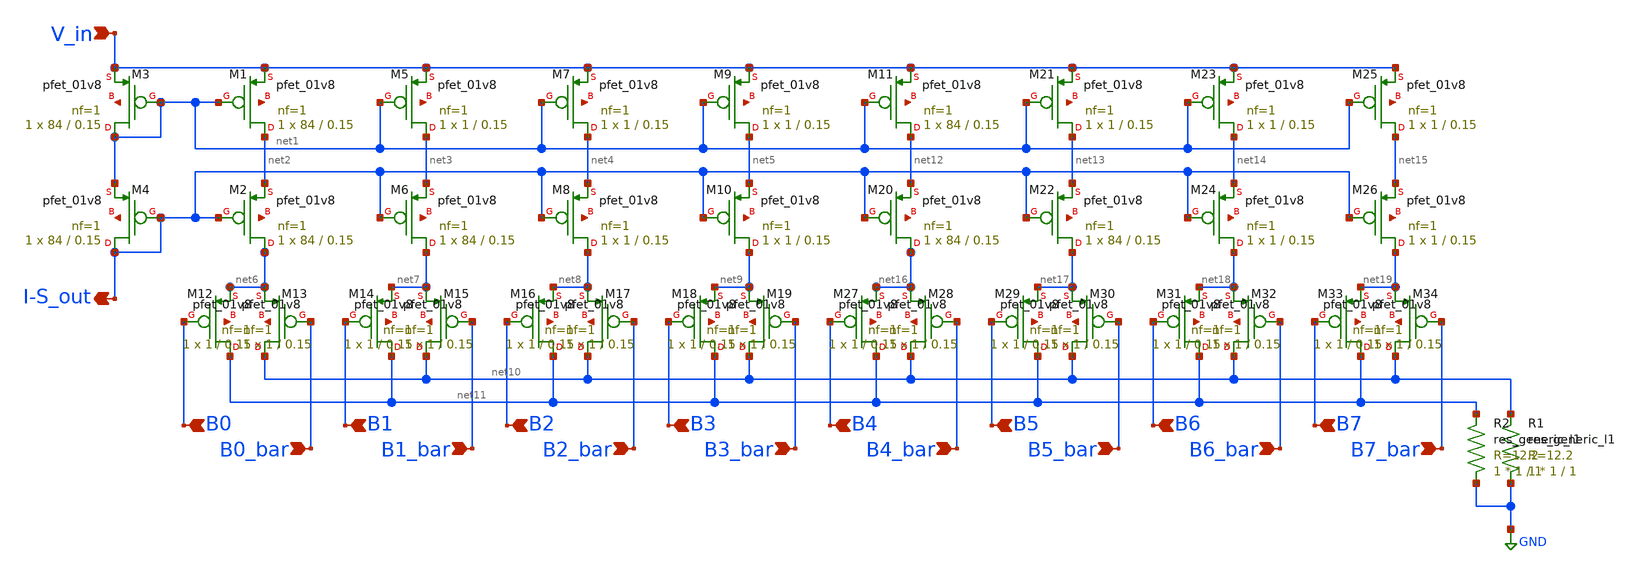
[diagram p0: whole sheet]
** sch_path: analog/schematics/DAC.sch
**.subckt DAC V_in I-S_out B0 V_in B0_bar B1 B2 B3 B1_bar B2_bar B3_bar B4 B4_bar B5 B6 B7 B5_bar
*+ B6_bar B7_bar
*.ipin V_in
*.opin I-S_out
*.ipin B0
*.ipin V_in
*.ipin B0_bar
*.ipin B1
*.ipin B2
*.ipin B3
*.ipin B1_bar
*.ipin B2_bar
*.ipin B3_bar
*.ipin B4
*.ipin B4_bar
*.ipin B5
*.ipin B6
*.ipin B7
*.ipin B5_bar
*.ipin B6_bar
*.ipin B7_bar
XM1 net2 net1 V_in net20 sky130_fd_pr__pfet_01v8 L=0.15 W=84 nf=1 ad='int((nf+1)/2) * W/nf * 0.29' as='int((nf+2)/2) * W/nf * 0.29'
+ pd='2*int((nf+1)/2) * (W/nf + 0.29)' ps='2*int((nf+2)/2) * (W/nf + 0.29)' nrd='0.29 / W' nrs='0.29 / W'
+ sa=0 sb=0 sd=0 mult=1 m=1
XM2 net6 I-S_out net2 net21 sky130_fd_pr__pfet_01v8 L=0.15 W=84 nf=1 ad='int((nf+1)/2) * W/nf * 0.29'
+ as='int((nf+2)/2) * W/nf * 0.29' pd='2*int((nf+1)/2) * (W/nf + 0.29)' ps='2*int((nf+2)/2) * (W/nf + 0.29)'
+ nrd='0.29 / W' nrs='0.29 / W' sa=0 sb=0 sd=0 mult=1 m=1
XM3 net1 net1 V_in net22 sky130_fd_pr__pfet_01v8 L=0.15 W=84 nf=1 ad='int((nf+1)/2) * W/nf * 0.29' as='int((nf+2)/2) * W/nf * 0.29'
+ pd='2*int((nf+1)/2) * (W/nf + 0.29)' ps='2*int((nf+2)/2) * (W/nf + 0.29)' nrd='0.29 / W' nrs='0.29 / W'
+ sa=0 sb=0 sd=0 mult=1 m=1
XM4 I-S_out I-S_out net1 net23 sky130_fd_pr__pfet_01v8 L=0.15 W=84 nf=1 ad='int((nf+1)/2) * W/nf * 0.29'
+ as='int((nf+2)/2) * W/nf * 0.29' pd='2*int((nf+1)/2) * (W/nf + 0.29)' ps='2*int((nf+2)/2) * (W/nf + 0.29)'
+ nrd='0.29 / W' nrs='0.29 / W' sa=0 sb=0 sd=0 mult=1 m=1
XM5 net3 net1 V_in net24 sky130_fd_pr__pfet_01v8 L=0.15 W=1 nf=1 ad='int((nf+1)/2) * W/nf * 0.29' as='int((nf+2)/2) * W/nf * 0.29'
+ pd='2*int((nf+1)/2) * (W/nf + 0.29)' ps='2*int((nf+2)/2) * (W/nf + 0.29)' nrd='0.29 / W' nrs='0.29 / W'
+ sa=0 sb=0 sd=0 mult=1 m=1
XM6 net7 I-S_out net3 net25 sky130_fd_pr__pfet_01v8 L=0.15 W=84 nf=1 ad='int((nf+1)/2) * W/nf * 0.29'
+ as='int((nf+2)/2) * W/nf * 0.29' pd='2*int((nf+1)/2) * (W/nf + 0.29)' ps='2*int((nf+2)/2) * (W/nf + 0.29)'
+ nrd='0.29 / W' nrs='0.29 / W' sa=0 sb=0 sd=0 mult=1 m=1
XM7 net4 net1 V_in net26 sky130_fd_pr__pfet_01v8 L=0.15 W=1 nf=1 ad='int((nf+1)/2) * W/nf * 0.29' as='int((nf+2)/2) * W/nf * 0.29'
+ pd='2*int((nf+1)/2) * (W/nf + 0.29)' ps='2*int((nf+2)/2) * (W/nf + 0.29)' nrd='0.29 / W' nrs='0.29 / W'
+ sa=0 sb=0 sd=0 mult=1 m=1
XM8 net8 I-S_out net4 net27 sky130_fd_pr__pfet_01v8 L=0.15 W=1 nf=1 ad='int((nf+1)/2) * W/nf * 0.29'
+ as='int((nf+2)/2) * W/nf * 0.29' pd='2*int((nf+1)/2) * (W/nf + 0.29)' ps='2*int((nf+2)/2) * (W/nf + 0.29)'
+ nrd='0.29 / W' nrs='0.29 / W' sa=0 sb=0 sd=0 mult=1 m=1
XM9 net5 net1 V_in net28 sky130_fd_pr__pfet_01v8 L=0.15 W=1 nf=1 ad='int((nf+1)/2) * W/nf * 0.29' as='int((nf+2)/2) * W/nf * 0.29'
+ pd='2*int((nf+1)/2) * (W/nf + 0.29)' ps='2*int((nf+2)/2) * (W/nf + 0.29)' nrd='0.29 / W' nrs='0.29 / W'
+ sa=0 sb=0 sd=0 mult=1 m=1
XM10 net9 I-S_out net5 net29 sky130_fd_pr__pfet_01v8 L=0.15 W=1 nf=1 ad='int((nf+1)/2) * W/nf * 0.29'
+ as='int((nf+2)/2) * W/nf * 0.29' pd='2*int((nf+1)/2) * (W/nf + 0.29)' ps='2*int((nf+2)/2) * (W/nf + 0.29)'
+ nrd='0.29 / W' nrs='0.29 / W' sa=0 sb=0 sd=0 mult=1 m=1
XM12 net11 B0 net6 net30 sky130_fd_pr__pfet_01v8 L=0.15 W=1 nf=1 ad='int((nf+1)/2) * W/nf * 0.29' as='int((nf+2)/2) * W/nf * 0.29'
+ pd='2*int((nf+1)/2) * (W/nf + 0.29)' ps='2*int((nf+2)/2) * (W/nf + 0.29)' nrd='0.29 / W' nrs='0.29 / W'
+ sa=0 sb=0 sd=0 mult=1 m=1
XM13 net10 B0_bar net6 net31 sky130_fd_pr__pfet_01v8 L=0.15 W=1 nf=1 ad='int((nf+1)/2) * W/nf * 0.29'
+ as='int((nf+2)/2) * W/nf * 0.29' pd='2*int((nf+1)/2) * (W/nf + 0.29)' ps='2*int((nf+2)/2) * (W/nf + 0.29)'
+ nrd='0.29 / W' nrs='0.29 / W' sa=0 sb=0 sd=0 mult=1 m=1
XM14 net11 B1 net7 net32 sky130_fd_pr__pfet_01v8 L=0.15 W=1 nf=1 ad='int((nf+1)/2) * W/nf * 0.29' as='int((nf+2)/2) * W/nf * 0.29'
+ pd='2*int((nf+1)/2) * (W/nf + 0.29)' ps='2*int((nf+2)/2) * (W/nf + 0.29)' nrd='0.29 / W' nrs='0.29 / W'
+ sa=0 sb=0 sd=0 mult=1 m=1
XM15 net10 B1_bar net7 net33 sky130_fd_pr__pfet_01v8 L=0.15 W=1 nf=1 ad='int((nf+1)/2) * W/nf * 0.29'
+ as='int((nf+2)/2) * W/nf * 0.29' pd='2*int((nf+1)/2) * (W/nf + 0.29)' ps='2*int((nf+2)/2) * (W/nf + 0.29)'
+ nrd='0.29 / W' nrs='0.29 / W' sa=0 sb=0 sd=0 mult=1 m=1
XM16 net11 B2 net8 net34 sky130_fd_pr__pfet_01v8 L=0.15 W=1 nf=1 ad='int((nf+1)/2) * W/nf * 0.29' as='int((nf+2)/2) * W/nf * 0.29'
+ pd='2*int((nf+1)/2) * (W/nf + 0.29)' ps='2*int((nf+2)/2) * (W/nf + 0.29)' nrd='0.29 / W' nrs='0.29 / W'
+ sa=0 sb=0 sd=0 mult=1 m=1
XM17 net10 B2_bar net8 net35 sky130_fd_pr__pfet_01v8 L=0.15 W=1 nf=1 ad='int((nf+1)/2) * W/nf * 0.29'
+ as='int((nf+2)/2) * W/nf * 0.29' pd='2*int((nf+1)/2) * (W/nf + 0.29)' ps='2*int((nf+2)/2) * (W/nf + 0.29)'
+ nrd='0.29 / W' nrs='0.29 / W' sa=0 sb=0 sd=0 mult=1 m=1
XM18 net11 B3 net9 net36 sky130_fd_pr__pfet_01v8 L=0.15 W=1 nf=1 ad='int((nf+1)/2) * W/nf * 0.29' as='int((nf+2)/2) * W/nf * 0.29'
+ pd='2*int((nf+1)/2) * (W/nf + 0.29)' ps='2*int((nf+2)/2) * (W/nf + 0.29)' nrd='0.29 / W' nrs='0.29 / W'
+ sa=0 sb=0 sd=0 mult=1 m=1
XM19 net10 B3_bar net9 net37 sky130_fd_pr__pfet_01v8 L=0.15 W=1 nf=1 ad='int((nf+1)/2) * W/nf * 0.29'
+ as='int((nf+2)/2) * W/nf * 0.29' pd='2*int((nf+1)/2) * (W/nf + 0.29)' ps='2*int((nf+2)/2) * (W/nf + 0.29)'
+ nrd='0.29 / W' nrs='0.29 / W' sa=0 sb=0 sd=0 mult=1 m=1
R1 GND net10 sky130_fd_pr__res_generic_l1 W=1 L=1 m=1
R2 GND net11 sky130_fd_pr__res_generic_l1 W=1 L=1 m=1
XM11 net12 net1 V_in net38 sky130_fd_pr__pfet_01v8 L=0.15 W=84 nf=1 ad='int((nf+1)/2) * W/nf * 0.29'
+ as='int((nf+2)/2) * W/nf * 0.29' pd='2*int((nf+1)/2) * (W/nf + 0.29)' ps='2*int((nf+2)/2) * (W/nf + 0.29)'
+ nrd='0.29 / W' nrs='0.29 / W' sa=0 sb=0 sd=0 mult=1 m=1
XM20 net16 I-S_out net12 net39 sky130_fd_pr__pfet_01v8 L=0.15 W=84 nf=1 ad='int((nf+1)/2) * W/nf * 0.29'
+ as='int((nf+2)/2) * W/nf * 0.29' pd='2*int((nf+1)/2) * (W/nf + 0.29)' ps='2*int((nf+2)/2) * (W/nf + 0.29)'
+ nrd='0.29 / W' nrs='0.29 / W' sa=0 sb=0 sd=0 mult=1 m=1
XM21 net13 net1 V_in net40 sky130_fd_pr__pfet_01v8 L=0.15 W=1 nf=1 ad='int((nf+1)/2) * W/nf * 0.29' as='int((nf+2)/2) * W/nf * 0.29'
+ pd='2*int((nf+1)/2) * (W/nf + 0.29)' ps='2*int((nf+2)/2) * (W/nf + 0.29)' nrd='0.29 / W' nrs='0.29 / W'
+ sa=0 sb=0 sd=0 mult=1 m=1
XM22 net17 I-S_out net13 net41 sky130_fd_pr__pfet_01v8 L=0.15 W=84 nf=1 ad='int((nf+1)/2) * W/nf * 0.29'
+ as='int((nf+2)/2) * W/nf * 0.29' pd='2*int((nf+1)/2) * (W/nf + 0.29)' ps='2*int((nf+2)/2) * (W/nf + 0.29)'
+ nrd='0.29 / W' nrs='0.29 / W' sa=0 sb=0 sd=0 mult=1 m=1
XM23 net14 net1 V_in net42 sky130_fd_pr__pfet_01v8 L=0.15 W=1 nf=1 ad='int((nf+1)/2) * W/nf * 0.29' as='int((nf+2)/2) * W/nf * 0.29'
+ pd='2*int((nf+1)/2) * (W/nf + 0.29)' ps='2*int((nf+2)/2) * (W/nf + 0.29)' nrd='0.29 / W' nrs='0.29 / W'
+ sa=0 sb=0 sd=0 mult=1 m=1
XM24 net18 I-S_out net14 net43 sky130_fd_pr__pfet_01v8 L=0.15 W=1 nf=1 ad='int((nf+1)/2) * W/nf * 0.29'
+ as='int((nf+2)/2) * W/nf * 0.29' pd='2*int((nf+1)/2) * (W/nf + 0.29)' ps='2*int((nf+2)/2) * (W/nf + 0.29)'
+ nrd='0.29 / W' nrs='0.29 / W' sa=0 sb=0 sd=0 mult=1 m=1
XM25 net15 net1 V_in net44 sky130_fd_pr__pfet_01v8 L=0.15 W=1 nf=1 ad='int((nf+1)/2) * W/nf * 0.29' as='int((nf+2)/2) * W/nf * 0.29'
+ pd='2*int((nf+1)/2) * (W/nf + 0.29)' ps='2*int((nf+2)/2) * (W/nf + 0.29)' nrd='0.29 / W' nrs='0.29 / W'
+ sa=0 sb=0 sd=0 mult=1 m=1
XM26 net19 I-S_out net15 net45 sky130_fd_pr__pfet_01v8 L=0.15 W=1 nf=1 ad='int((nf+1)/2) * W/nf * 0.29'
+ as='int((nf+2)/2) * W/nf * 0.29' pd='2*int((nf+1)/2) * (W/nf + 0.29)' ps='2*int((nf+2)/2) * (W/nf + 0.29)'
+ nrd='0.29 / W' nrs='0.29 / W' sa=0 sb=0 sd=0 mult=1 m=1
XM27 net11 B4 net16 net46 sky130_fd_pr__pfet_01v8 L=0.15 W=1 nf=1 ad='int((nf+1)/2) * W/nf * 0.29' as='int((nf+2)/2) * W/nf * 0.29'
+ pd='2*int((nf+1)/2) * (W/nf + 0.29)' ps='2*int((nf+2)/2) * (W/nf + 0.29)' nrd='0.29 / W' nrs='0.29 / W'
+ sa=0 sb=0 sd=0 mult=1 m=1
XM28 net10 B4_bar net16 net47 sky130_fd_pr__pfet_01v8 L=0.15 W=1 nf=1 ad='int((nf+1)/2) * W/nf * 0.29'
+ as='int((nf+2)/2) * W/nf * 0.29' pd='2*int((nf+1)/2) * (W/nf + 0.29)' ps='2*int((nf+2)/2) * (W/nf + 0.29)'
+ nrd='0.29 / W' nrs='0.29 / W' sa=0 sb=0 sd=0 mult=1 m=1
XM29 net11 B5 net17 net48 sky130_fd_pr__pfet_01v8 L=0.15 W=1 nf=1 ad='int((nf+1)/2) * W/nf * 0.29' as='int((nf+2)/2) * W/nf * 0.29'
+ pd='2*int((nf+1)/2) * (W/nf + 0.29)' ps='2*int((nf+2)/2) * (W/nf + 0.29)' nrd='0.29 / W' nrs='0.29 / W'
+ sa=0 sb=0 sd=0 mult=1 m=1
XM30 net10 B5_bar net17 net49 sky130_fd_pr__pfet_01v8 L=0.15 W=1 nf=1 ad='int((nf+1)/2) * W/nf * 0.29'
+ as='int((nf+2)/2) * W/nf * 0.29' pd='2*int((nf+1)/2) * (W/nf + 0.29)' ps='2*int((nf+2)/2) * (W/nf + 0.29)'
+ nrd='0.29 / W' nrs='0.29 / W' sa=0 sb=0 sd=0 mult=1 m=1
XM31 net11 B6 net18 net50 sky130_fd_pr__pfet_01v8 L=0.15 W=1 nf=1 ad='int((nf+1)/2) * W/nf * 0.29' as='int((nf+2)/2) * W/nf * 0.29'
+ pd='2*int((nf+1)/2) * (W/nf + 0.29)' ps='2*int((nf+2)/2) * (W/nf + 0.29)' nrd='0.29 / W' nrs='0.29 / W'
+ sa=0 sb=0 sd=0 mult=1 m=1
XM32 net10 B6_bar net18 net51 sky130_fd_pr__pfet_01v8 L=0.15 W=1 nf=1 ad='int((nf+1)/2) * W/nf * 0.29'
+ as='int((nf+2)/2) * W/nf * 0.29' pd='2*int((nf+1)/2) * (W/nf + 0.29)' ps='2*int((nf+2)/2) * (W/nf + 0.29)'
+ nrd='0.29 / W' nrs='0.29 / W' sa=0 sb=0 sd=0 mult=1 m=1
XM33 net11 B7 net19 net52 sky130_fd_pr__pfet_01v8 L=0.15 W=1 nf=1 ad='int((nf+1)/2) * W/nf * 0.29' as='int((nf+2)/2) * W/nf * 0.29'
+ pd='2*int((nf+1)/2) * (W/nf + 0.29)' ps='2*int((nf+2)/2) * (W/nf + 0.29)' nrd='0.29 / W' nrs='0.29 / W'
+ sa=0 sb=0 sd=0 mult=1 m=1
XM34 net10 B7_bar net19 net53 sky130_fd_pr__pfet_01v8 L=0.15 W=1 nf=1 ad='int((nf+1)/2) * W/nf * 0.29'
+ as='int((nf+2)/2) * W/nf * 0.29' pd='2*int((nf+1)/2) * (W/nf + 0.29)' ps='2*int((nf+2)/2) * (W/nf + 0.29)'
+ nrd='0.29 / W' nrs='0.29 / W' sa=0 sb=0 sd=0 mult=1 m=1
**.ends
.GLOBAL GND
.end
